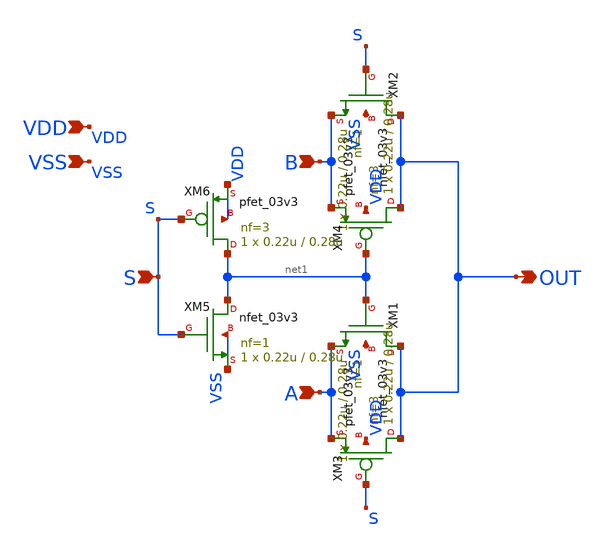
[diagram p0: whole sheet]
** sch_path: tests/ptl_mux/xschem/ptl_mux.sch
**.subckt ptl_mux OUT S B A VDD VSS
*.opin OUT
*.ipin S
*.ipin B
*.ipin A
*.ipin VDD
*.ipin VSS
XM2 OUT S B VSS nfet_03v3 L=0.28u W=0.22u nf=1 ad='int((nf+1)/2) * W/nf * 0.18u' as='int((nf+2)/2) * W/nf * 0.18u'
+ pd='2*int((nf+1)/2) * (W/nf + 0.18u)' ps='2*int((nf+2)/2) * (W/nf + 0.18u)' nrd='0.18u / W' nrs='0.18u / W'
+ sa=0 sb=0 sd=0 m=1
XM1 OUT net1 A VSS nfet_03v3 L=0.28u W=0.22u nf=1 ad='int((nf+1)/2) * W/nf * 0.18u' as='int((nf+2)/2) * W/nf * 0.18u'
+ pd='2*int((nf+1)/2) * (W/nf + 0.18u)' ps='2*int((nf+2)/2) * (W/nf + 0.18u)' nrd='0.18u / W' nrs='0.18u / W'
+ sa=0 sb=0 sd=0 m=1
XM4 OUT net1 B VDD pfet_03v3 L=0.28u W=0.22u nf=3 ad='int((nf+1)/2) * W/nf * 0.18u' as='int((nf+2)/2) * W/nf * 0.18u'
+ pd='2*int((nf+1)/2) * (W/nf + 0.18u)' ps='2*int((nf+2)/2) * (W/nf + 0.18u)' nrd='0.18u / W' nrs='0.18u / W'
+ sa=0 sb=0 sd=0 m=1
XM3 OUT S A VDD pfet_03v3 L=0.28u W=0.22u nf=3 ad='int((nf+1)/2) * W/nf * 0.18u' as='int((nf+2)/2) * W/nf * 0.18u'
+ pd='2*int((nf+1)/2) * (W/nf + 0.18u)' ps='2*int((nf+2)/2) * (W/nf + 0.18u)' nrd='0.18u / W' nrs='0.18u / W'
+ sa=0 sb=0 sd=0 m=1
XM5 net1 S VSS VSS nfet_03v3 L=0.28u W=0.22u nf=1 ad='int((nf+1)/2) * W/nf * 0.18u' as='int((nf+2)/2) * W/nf * 0.18u'
+ pd='2*int((nf+1)/2) * (W/nf + 0.18u)' ps='2*int((nf+2)/2) * (W/nf + 0.18u)' nrd='0.18u / W' nrs='0.18u / W'
+ sa=0 sb=0 sd=0 m=1
XM6 net1 S VDD VDD pfet_03v3 L=0.28u W=0.22u nf=3 ad='int((nf+1)/2) * W/nf * 0.18u' as='int((nf+2)/2) * W/nf * 0.18u'
+ pd='2*int((nf+1)/2) * (W/nf + 0.18u)' ps='2*int((nf+2)/2) * (W/nf + 0.18u)' nrd='0.18u / W' nrs='0.18u / W'
+ sa=0 sb=0 sd=0 m=1
**.ends
.end
